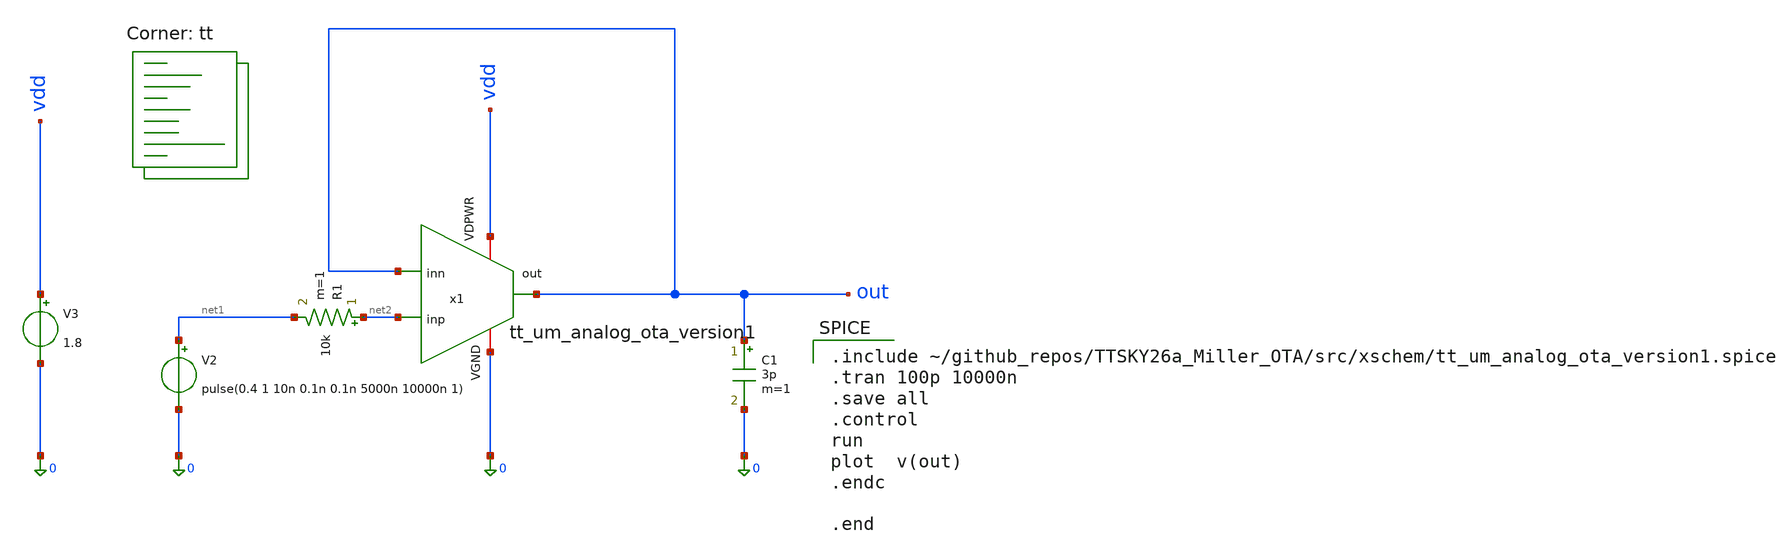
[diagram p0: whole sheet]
** sch_path: src/xschem/miller_ota_postLayout_test_trans.sch
**.subckt miller_ota_postLayout_test_trans
V2 net1 0 pulse(0.4 1 10n 0.1n 0.1n 5000n 10000n 1)
R1 net2 net1 10k m=1
C1 out 0 3p m=1
V3 vdd 0 1.8
x1 vdd out out net2 0 tt_um_analog_ota_version1
**** begin user architecture code

.include ~/github_repos/TTSKY26a_Miller_OTA/src/xschem/tt_um_analog_ota_version1.spice
.tran 100p 10000n
.save all
.control
run
plot  v(out)
.endc

.end

.lib $::SKYWATER_MODELS/sky130.lib.spice tt
**** end user architecture code
**.ends
.end
